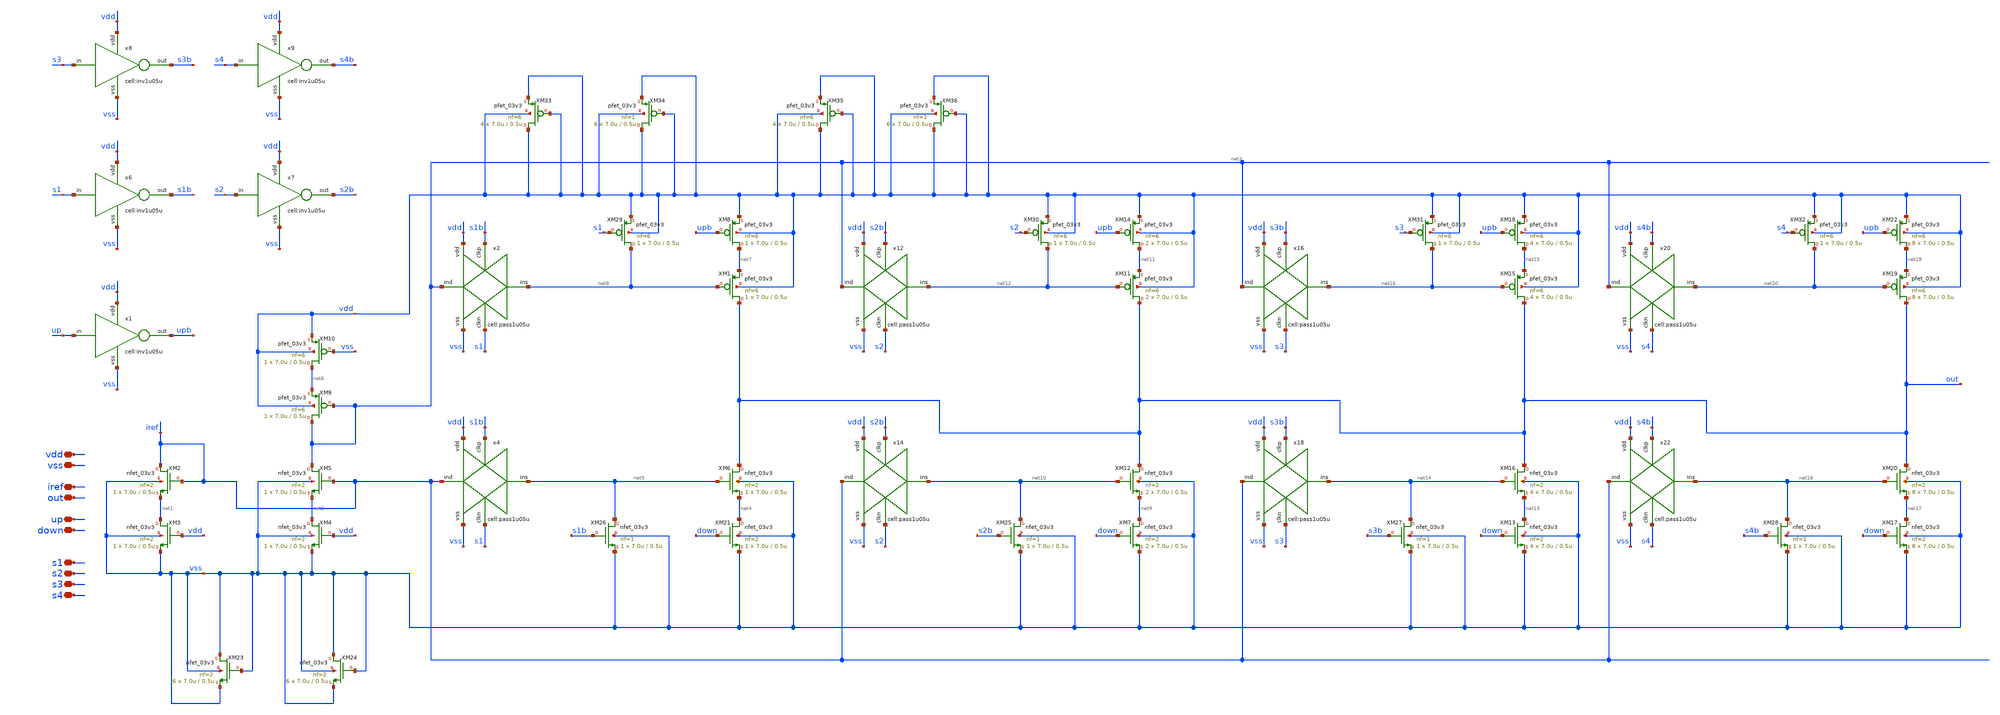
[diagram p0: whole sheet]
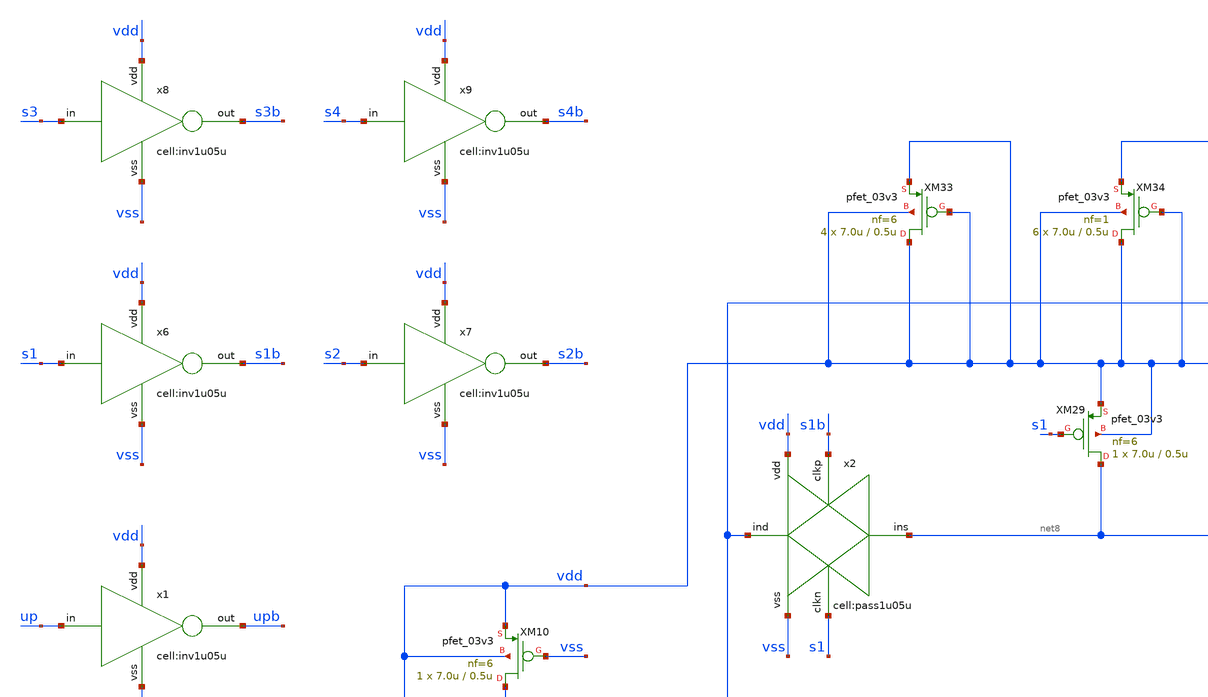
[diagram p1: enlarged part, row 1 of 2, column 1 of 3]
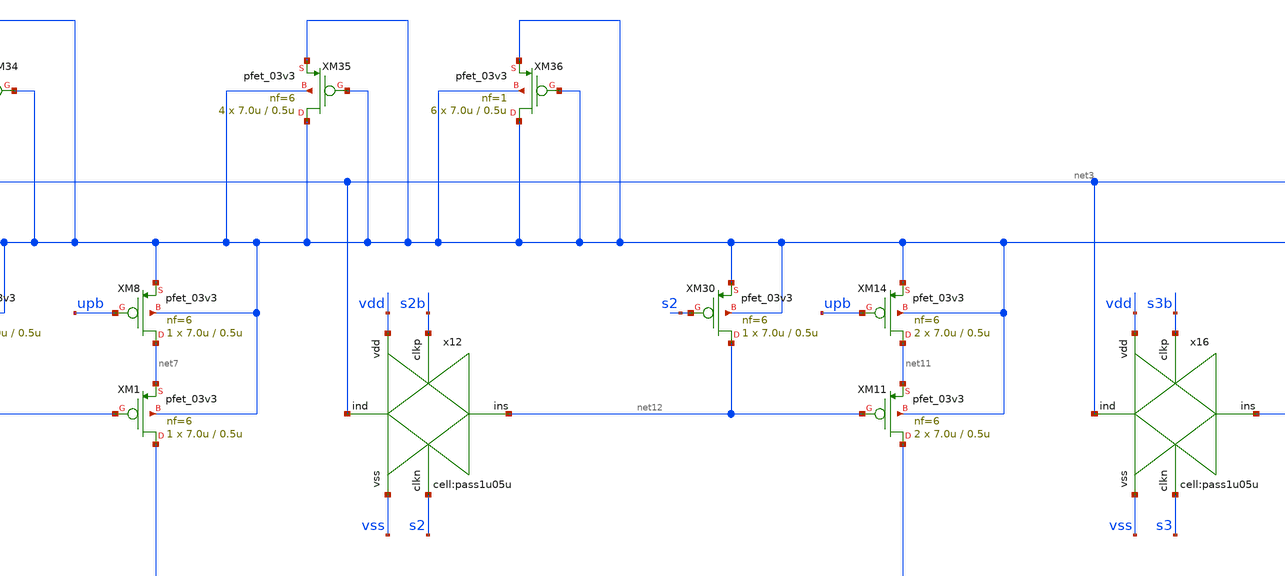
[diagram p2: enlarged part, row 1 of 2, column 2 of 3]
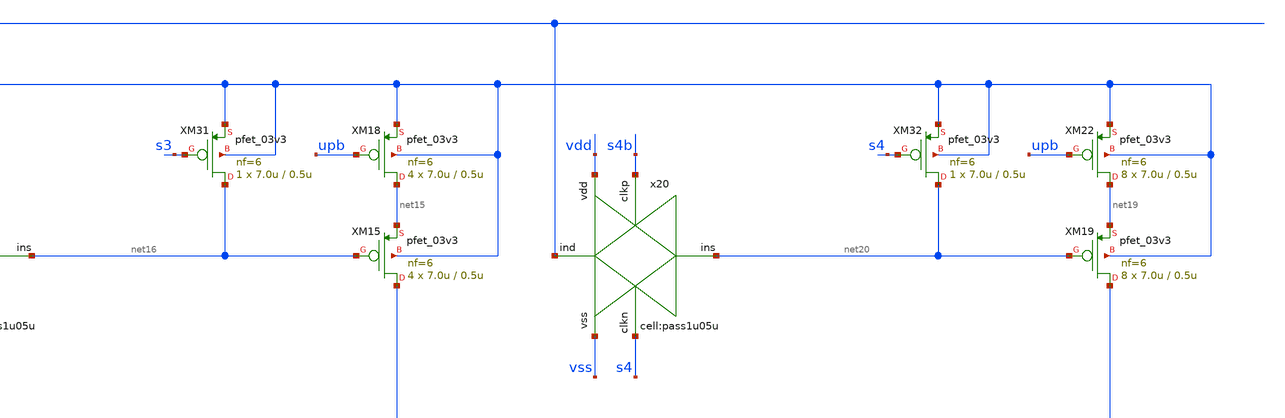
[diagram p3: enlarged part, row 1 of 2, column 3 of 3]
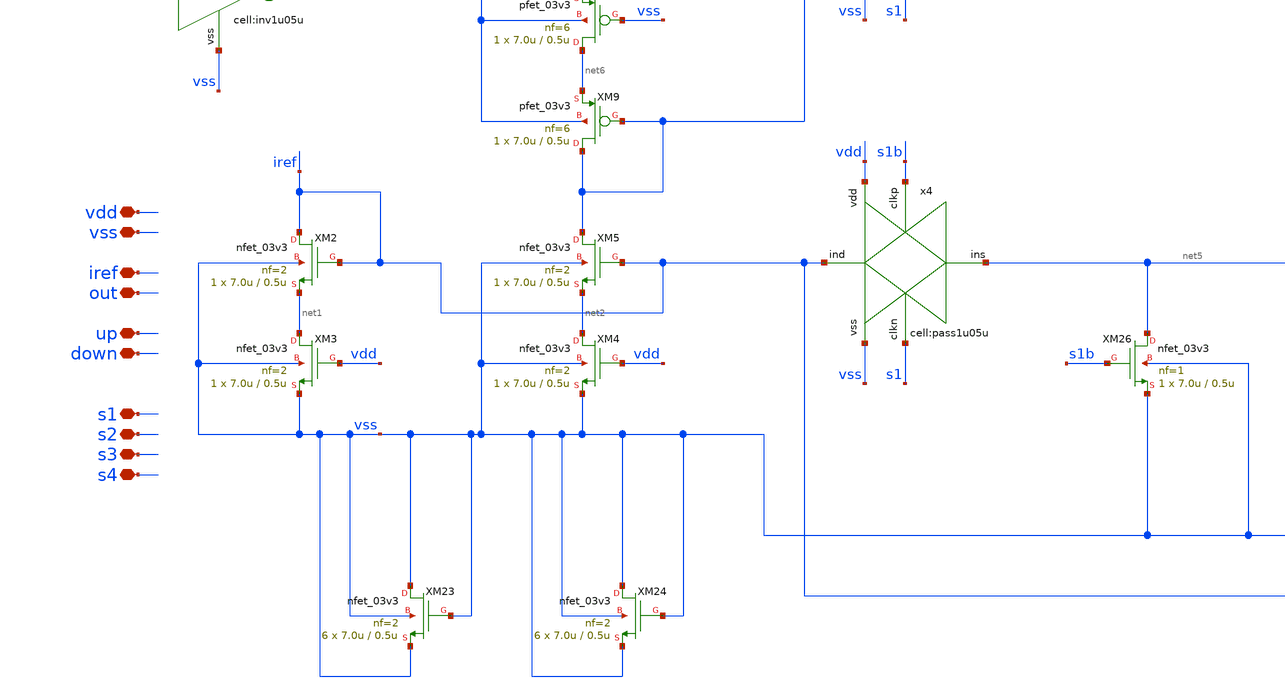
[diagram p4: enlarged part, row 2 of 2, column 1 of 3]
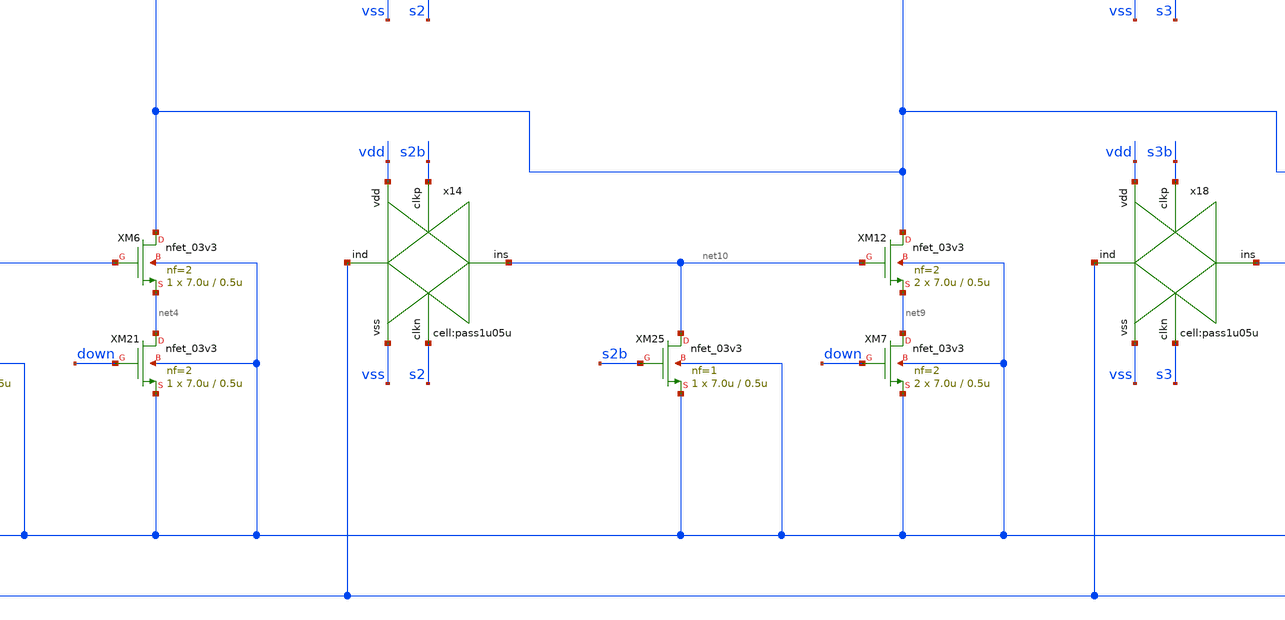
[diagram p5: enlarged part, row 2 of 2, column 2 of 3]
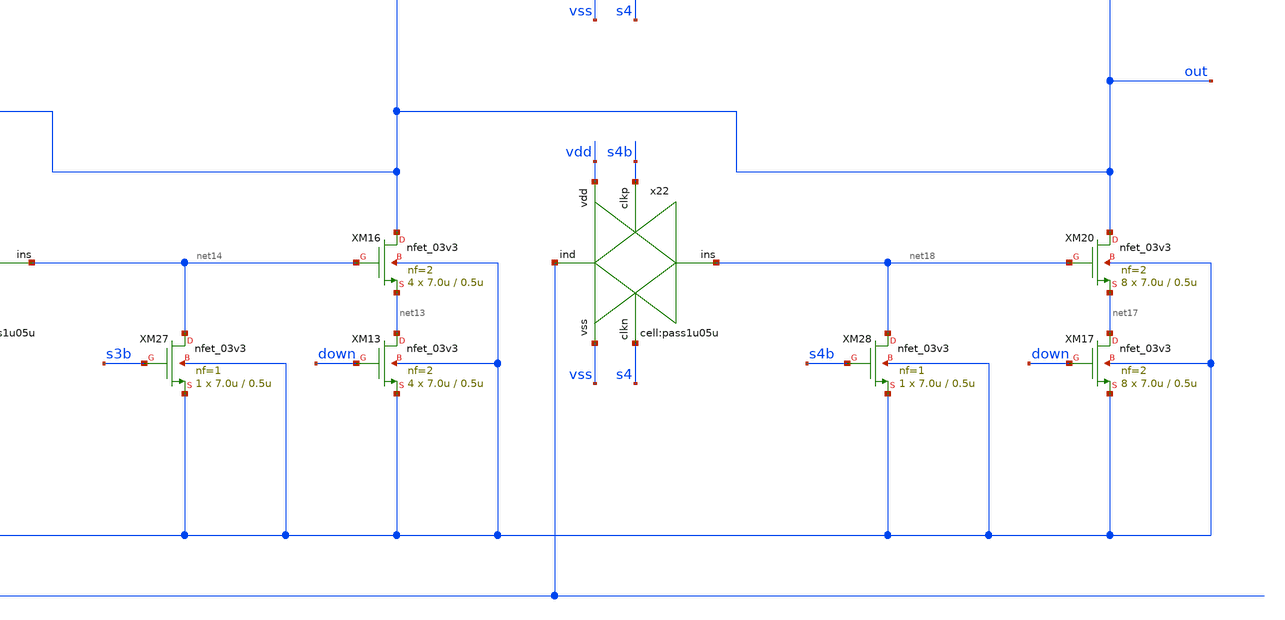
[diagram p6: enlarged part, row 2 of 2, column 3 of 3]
** sch_path: designs/libs/xp_core_analog/xp_programmable_basic_pump/xp_programmable_basic_pump.sch
**.subckt xp_programmable_basic_pump vdd vss up down iref out s3 s4 s1 s2
*.iopin vdd
*.iopin vss
*.iopin up
*.iopin down
*.iopin iref
*.iopin out
*.iopin s3
*.iopin s4
*.iopin s1
*.iopin s2
XM6 out net5 net4 vss nfet_03v3 L=0.5u W=7.0u nf=2 ad='int((nf+1)/2) * W/nf * 0.18u' as='int((nf+2)/2) * W/nf * 0.18u'
+ pd='2*int((nf+1)/2) * (W/nf + 0.18u)' ps='2*int((nf+2)/2) * (W/nf + 0.18u)' nrd='0.18u / W' nrs='0.18u / W'
+ sa=0 sb=0 sd=0 m=1
XM8 net7 upb vdd vdd pfet_03v3 L=0.5u W=7.0u nf=6 ad='int((nf+1)/2) * W/nf * 0.18u' as='int((nf+2)/2) * W/nf * 0.18u'
+ pd='2*int((nf+1)/2) * (W/nf + 0.18u)' ps='2*int((nf+2)/2) * (W/nf + 0.18u)' nrd='0.18u / W' nrs='0.18u / W'
+ sa=0 sb=0 sd=0 m=1
XM10 net6 vss vdd vdd pfet_03v3 L=0.5u W=7.0u nf=6 ad='int((nf+1)/2) * W/nf * 0.18u' as='int((nf+2)/2) * W/nf * 0.18u'
+ pd='2*int((nf+1)/2) * (W/nf + 0.18u)' ps='2*int((nf+2)/2) * (W/nf + 0.18u)' nrd='0.18u / W' nrs='0.18u / W'
+ sa=0 sb=0 sd=0 m=1
x1 up vdd upb vss inv1u05u
x2 net3 vss s1 net8 s1b vdd pass1u05u
x4 iref vss s1 net5 s1b vdd pass1u05u
x6 s1 vdd s1b vss inv1u05u
x7 s2 vdd s2b vss inv1u05u
x8 s3 vdd s3b vss inv1u05u
x9 s4 vdd s4b vss inv1u05u
XM12 out net10 net9 vss nfet_03v3 L=0.5u W=7.0u nf=2 ad='int((nf+1)/2) * W/nf * 0.18u' as='int((nf+2)/2) * W/nf * 0.18u'
+ pd='2*int((nf+1)/2) * (W/nf + 0.18u)' ps='2*int((nf+2)/2) * (W/nf + 0.18u)' nrd='0.18u / W' nrs='0.18u / W'
+ sa=0 sb=0 sd=0 m=2
XM14 net11 upb vdd vdd pfet_03v3 L=0.5u W=7.0u nf=6 ad='int((nf+1)/2) * W/nf * 0.18u' as='int((nf+2)/2) * W/nf * 0.18u'
+ pd='2*int((nf+1)/2) * (W/nf + 0.18u)' ps='2*int((nf+2)/2) * (W/nf + 0.18u)' nrd='0.18u / W' nrs='0.18u / W'
+ sa=0 sb=0 sd=0 m=2
x12 net3 vss s2 net12 s2b vdd pass1u05u
x14 iref vss s2 net10 s2b vdd pass1u05u
XM16 out net14 net13 vss nfet_03v3 L=0.5u W=7.0u nf=2 ad='int((nf+1)/2) * W/nf * 0.18u' as='int((nf+2)/2) * W/nf * 0.18u'
+ pd='2*int((nf+1)/2) * (W/nf + 0.18u)' ps='2*int((nf+2)/2) * (W/nf + 0.18u)' nrd='0.18u / W' nrs='0.18u / W'
+ sa=0 sb=0 sd=0 m=4
XM18 net15 upb vdd vdd pfet_03v3 L=0.5u W=7.0u nf=6 ad='int((nf+1)/2) * W/nf * 0.18u' as='int((nf+2)/2) * W/nf * 0.18u'
+ pd='2*int((nf+1)/2) * (W/nf + 0.18u)' ps='2*int((nf+2)/2) * (W/nf + 0.18u)' nrd='0.18u / W' nrs='0.18u / W'
+ sa=0 sb=0 sd=0 m=4
x16 net3 vss s3 net16 s3b vdd pass1u05u
x18 iref vss s3 net14 s3b vdd pass1u05u
XM19 out net20 net19 vdd pfet_03v3 L=0.5u W=7.0u nf=6 ad='int((nf+1)/2) * W/nf * 0.18u' as='int((nf+2)/2) * W/nf * 0.18u'
+ pd='2*int((nf+1)/2) * (W/nf + 0.18u)' ps='2*int((nf+2)/2) * (W/nf + 0.18u)' nrd='0.18u / W' nrs='0.18u / W'
+ sa=0 sb=0 sd=0 m=8
XM20 out net18 net17 vss nfet_03v3 L=0.5u W=7.0u nf=2 ad='int((nf+1)/2) * W/nf * 0.18u' as='int((nf+2)/2) * W/nf * 0.18u'
+ pd='2*int((nf+1)/2) * (W/nf + 0.18u)' ps='2*int((nf+2)/2) * (W/nf + 0.18u)' nrd='0.18u / W' nrs='0.18u / W'
+ sa=0 sb=0 sd=0 m=8
XM22 net19 upb vdd vdd pfet_03v3 L=0.5u W=7.0u nf=6 ad='int((nf+1)/2) * W/nf * 0.18u' as='int((nf+2)/2) * W/nf * 0.18u'
+ pd='2*int((nf+1)/2) * (W/nf + 0.18u)' ps='2*int((nf+2)/2) * (W/nf + 0.18u)' nrd='0.18u / W' nrs='0.18u / W'
+ sa=0 sb=0 sd=0 m=8
x20 net3 vss s4 net20 s4b vdd pass1u05u
x22 iref vss s4 net18 s4b vdd pass1u05u
XM2 iref iref net1 vss nfet_03v3 L=0.5u W=7.0u nf=2 ad='int((nf+1)/2) * W/nf * 0.18u' as='int((nf+2)/2) * W/nf * 0.18u'
+ pd='2*int((nf+1)/2) * (W/nf + 0.18u)' ps='2*int((nf+2)/2) * (W/nf + 0.18u)' nrd='0.18u / W' nrs='0.18u / W'
+ sa=0 sb=0 sd=0 m=1
XM9 net3 net3 net6 vdd pfet_03v3 L=0.5u W=7.0u nf=6 ad='int((nf+1)/2) * W/nf * 0.18u' as='int((nf+2)/2) * W/nf * 0.18u'
+ pd='2*int((nf+1)/2) * (W/nf + 0.18u)' ps='2*int((nf+2)/2) * (W/nf + 0.18u)' nrd='0.18u / W' nrs='0.18u / W'
+ sa=0 sb=0 sd=0 m=1
XM1 out net8 net7 vdd pfet_03v3 L=0.5u W=7.0u nf=6 ad='int((nf+1)/2) * W/nf * 0.18u' as='int((nf+2)/2) * W/nf * 0.18u'
+ pd='2*int((nf+1)/2) * (W/nf + 0.18u)' ps='2*int((nf+2)/2) * (W/nf + 0.18u)' nrd='0.18u / W' nrs='0.18u / W'
+ sa=0 sb=0 sd=0 m=1
XM11 out net12 net11 vdd pfet_03v3 L=0.5u W=7.0u nf=6 ad='int((nf+1)/2) * W/nf * 0.18u' as='int((nf+2)/2) * W/nf * 0.18u'
+ pd='2*int((nf+1)/2) * (W/nf + 0.18u)' ps='2*int((nf+2)/2) * (W/nf + 0.18u)' nrd='0.18u / W' nrs='0.18u / W'
+ sa=0 sb=0 sd=0 m=2
XM15 out net16 net15 vdd pfet_03v3 L=0.5u W=7.0u nf=6 ad='int((nf+1)/2) * W/nf * 0.18u' as='int((nf+2)/2) * W/nf * 0.18u'
+ pd='2*int((nf+1)/2) * (W/nf + 0.18u)' ps='2*int((nf+2)/2) * (W/nf + 0.18u)' nrd='0.18u / W' nrs='0.18u / W'
+ sa=0 sb=0 sd=0 m=4
XM3 net1 vdd vss vss nfet_03v3 L=0.5u W=7.0u nf=2 ad='int((nf+1)/2) * W/nf * 0.18u' as='int((nf+2)/2) * W/nf * 0.18u'
+ pd='2*int((nf+1)/2) * (W/nf + 0.18u)' ps='2*int((nf+2)/2) * (W/nf + 0.18u)' nrd='0.18u / W' nrs='0.18u / W'
+ sa=0 sb=0 sd=0 m=1
XM4 net2 vdd vss vss nfet_03v3 L=0.5u W=7.0u nf=2 ad='int((nf+1)/2) * W/nf * 0.18u' as='int((nf+2)/2) * W/nf * 0.18u'
+ pd='2*int((nf+1)/2) * (W/nf + 0.18u)' ps='2*int((nf+2)/2) * (W/nf + 0.18u)' nrd='0.18u / W' nrs='0.18u / W'
+ sa=0 sb=0 sd=0 m=1
XM5 net3 iref net2 vss nfet_03v3 L=0.5u W=7.0u nf=2 ad='int((nf+1)/2) * W/nf * 0.18u' as='int((nf+2)/2) * W/nf * 0.18u'
+ pd='2*int((nf+1)/2) * (W/nf + 0.18u)' ps='2*int((nf+2)/2) * (W/nf + 0.18u)' nrd='0.18u / W' nrs='0.18u / W'
+ sa=0 sb=0 sd=0 m=1
XM21 net4 down vss vss nfet_03v3 L=0.5u W=7.0u nf=2 ad='int((nf+1)/2) * W/nf * 0.18u' as='int((nf+2)/2) * W/nf * 0.18u'
+ pd='2*int((nf+1)/2) * (W/nf + 0.18u)' ps='2*int((nf+2)/2) * (W/nf + 0.18u)' nrd='0.18u / W' nrs='0.18u / W'
+ sa=0 sb=0 sd=0 m=1
XM7 net9 down vss vss nfet_03v3 L=0.5u W=7.0u nf=2 ad='int((nf+1)/2) * W/nf * 0.18u' as='int((nf+2)/2) * W/nf * 0.18u'
+ pd='2*int((nf+1)/2) * (W/nf + 0.18u)' ps='2*int((nf+2)/2) * (W/nf + 0.18u)' nrd='0.18u / W' nrs='0.18u / W'
+ sa=0 sb=0 sd=0 m=2
XM13 net13 down vss vss nfet_03v3 L=0.5u W=7.0u nf=2 ad='int((nf+1)/2) * W/nf * 0.18u' as='int((nf+2)/2) * W/nf * 0.18u'
+ pd='2*int((nf+1)/2) * (W/nf + 0.18u)' ps='2*int((nf+2)/2) * (W/nf + 0.18u)' nrd='0.18u / W' nrs='0.18u / W'
+ sa=0 sb=0 sd=0 m=4
XM17 net17 down vss vss nfet_03v3 L=0.5u W=7.0u nf=2 ad='int((nf+1)/2) * W/nf * 0.18u' as='int((nf+2)/2) * W/nf * 0.18u'
+ pd='2*int((nf+1)/2) * (W/nf + 0.18u)' ps='2*int((nf+2)/2) * (W/nf + 0.18u)' nrd='0.18u / W' nrs='0.18u / W'
+ sa=0 sb=0 sd=0 m=8
XM23 vss vss vss vss nfet_03v3 L=0.5u W=7.0u nf=2 ad='int((nf+1)/2) * W/nf * 0.18u' as='int((nf+2)/2) * W/nf * 0.18u'
+ pd='2*int((nf+1)/2) * (W/nf + 0.18u)' ps='2*int((nf+2)/2) * (W/nf + 0.18u)' nrd='0.18u / W' nrs='0.18u / W'
+ sa=0 sb=0 sd=0 m=6
XM24 vss vss vss vss nfet_03v3 L=0.5u W=7.0u nf=2 ad='int((nf+1)/2) * W/nf * 0.18u' as='int((nf+2)/2) * W/nf * 0.18u'
+ pd='2*int((nf+1)/2) * (W/nf + 0.18u)' ps='2*int((nf+2)/2) * (W/nf + 0.18u)' nrd='0.18u / W' nrs='0.18u / W'
+ sa=0 sb=0 sd=0 m=6
XM25 net10 s2b vss vss nfet_03v3 L=0.5u W=7.0u nf=1 ad='int((nf+1)/2) * W/nf * 0.18u' as='int((nf+2)/2) * W/nf * 0.18u'
+ pd='2*int((nf+1)/2) * (W/nf + 0.18u)' ps='2*int((nf+2)/2) * (W/nf + 0.18u)' nrd='0.18u / W' nrs='0.18u / W'
+ sa=0 sb=0 sd=0 m=1
XM26 net5 s1b vss vss nfet_03v3 L=0.5u W=7.0u nf=1 ad='int((nf+1)/2) * W/nf * 0.18u' as='int((nf+2)/2) * W/nf * 0.18u'
+ pd='2*int((nf+1)/2) * (W/nf + 0.18u)' ps='2*int((nf+2)/2) * (W/nf + 0.18u)' nrd='0.18u / W' nrs='0.18u / W'
+ sa=0 sb=0 sd=0 m=1
XM27 net14 s3b vss vss nfet_03v3 L=0.5u W=7.0u nf=1 ad='int((nf+1)/2) * W/nf * 0.18u' as='int((nf+2)/2) * W/nf * 0.18u'
+ pd='2*int((nf+1)/2) * (W/nf + 0.18u)' ps='2*int((nf+2)/2) * (W/nf + 0.18u)' nrd='0.18u / W' nrs='0.18u / W'
+ sa=0 sb=0 sd=0 m=1
XM28 net18 s4b vss vss nfet_03v3 L=0.5u W=7.0u nf=1 ad='int((nf+1)/2) * W/nf * 0.18u' as='int((nf+2)/2) * W/nf * 0.18u'
+ pd='2*int((nf+1)/2) * (W/nf + 0.18u)' ps='2*int((nf+2)/2) * (W/nf + 0.18u)' nrd='0.18u / W' nrs='0.18u / W'
+ sa=0 sb=0 sd=0 m=1
XM29 net8 s1 vdd vdd pfet_03v3 L=0.5u W=7.0u nf=6 ad='int((nf+1)/2) * W/nf * 0.18u' as='int((nf+2)/2) * W/nf * 0.18u'
+ pd='2*int((nf+1)/2) * (W/nf + 0.18u)' ps='2*int((nf+2)/2) * (W/nf + 0.18u)' nrd='0.18u / W' nrs='0.18u / W'
+ sa=0 sb=0 sd=0 m=1
XM30 net12 s2 vdd vdd pfet_03v3 L=0.5u W=7.0u nf=6 ad='int((nf+1)/2) * W/nf * 0.18u' as='int((nf+2)/2) * W/nf * 0.18u'
+ pd='2*int((nf+1)/2) * (W/nf + 0.18u)' ps='2*int((nf+2)/2) * (W/nf + 0.18u)' nrd='0.18u / W' nrs='0.18u / W'
+ sa=0 sb=0 sd=0 m=1
XM31 net16 s3 vdd vdd pfet_03v3 L=0.5u W=7.0u nf=6 ad='int((nf+1)/2) * W/nf * 0.18u' as='int((nf+2)/2) * W/nf * 0.18u'
+ pd='2*int((nf+1)/2) * (W/nf + 0.18u)' ps='2*int((nf+2)/2) * (W/nf + 0.18u)' nrd='0.18u / W' nrs='0.18u / W'
+ sa=0 sb=0 sd=0 m=1
XM32 net20 s4 vdd vdd pfet_03v3 L=0.5u W=7.0u nf=6 ad='int((nf+1)/2) * W/nf * 0.18u' as='int((nf+2)/2) * W/nf * 0.18u'
+ pd='2*int((nf+1)/2) * (W/nf + 0.18u)' ps='2*int((nf+2)/2) * (W/nf + 0.18u)' nrd='0.18u / W' nrs='0.18u / W'
+ sa=0 sb=0 sd=0 m=1
XM33 vdd vdd vdd vdd pfet_03v3 L=0.5u W=7.0u nf=6 ad='int((nf+1)/2) * W/nf * 0.18u' as='int((nf+2)/2) * W/nf * 0.18u'
+ pd='2*int((nf+1)/2) * (W/nf + 0.18u)' ps='2*int((nf+2)/2) * (W/nf + 0.18u)' nrd='0.18u / W' nrs='0.18u / W'
+ sa=0 sb=0 sd=0 m=4
XM34 vdd vdd vdd vdd pfet_03v3 L=0.5u W=7.0u nf=1 ad='int((nf+1)/2) * W/nf * 0.18u' as='int((nf+2)/2) * W/nf * 0.18u'
+ pd='2*int((nf+1)/2) * (W/nf + 0.18u)' ps='2*int((nf+2)/2) * (W/nf + 0.18u)' nrd='0.18u / W' nrs='0.18u / W'
+ sa=0 sb=0 sd=0 m=6
XM35 vdd vdd vdd vdd pfet_03v3 L=0.5u W=7.0u nf=6 ad='int((nf+1)/2) * W/nf * 0.18u' as='int((nf+2)/2) * W/nf * 0.18u'
+ pd='2*int((nf+1)/2) * (W/nf + 0.18u)' ps='2*int((nf+2)/2) * (W/nf + 0.18u)' nrd='0.18u / W' nrs='0.18u / W'
+ sa=0 sb=0 sd=0 m=4
XM36 vdd vdd vdd vdd pfet_03v3 L=0.5u W=7.0u nf=1 ad='int((nf+1)/2) * W/nf * 0.18u' as='int((nf+2)/2) * W/nf * 0.18u'
+ pd='2*int((nf+1)/2) * (W/nf + 0.18u)' ps='2*int((nf+2)/2) * (W/nf + 0.18u)' nrd='0.18u / W' nrs='0.18u / W'
+ sa=0 sb=0 sd=0 m=6
**.ends
.end
